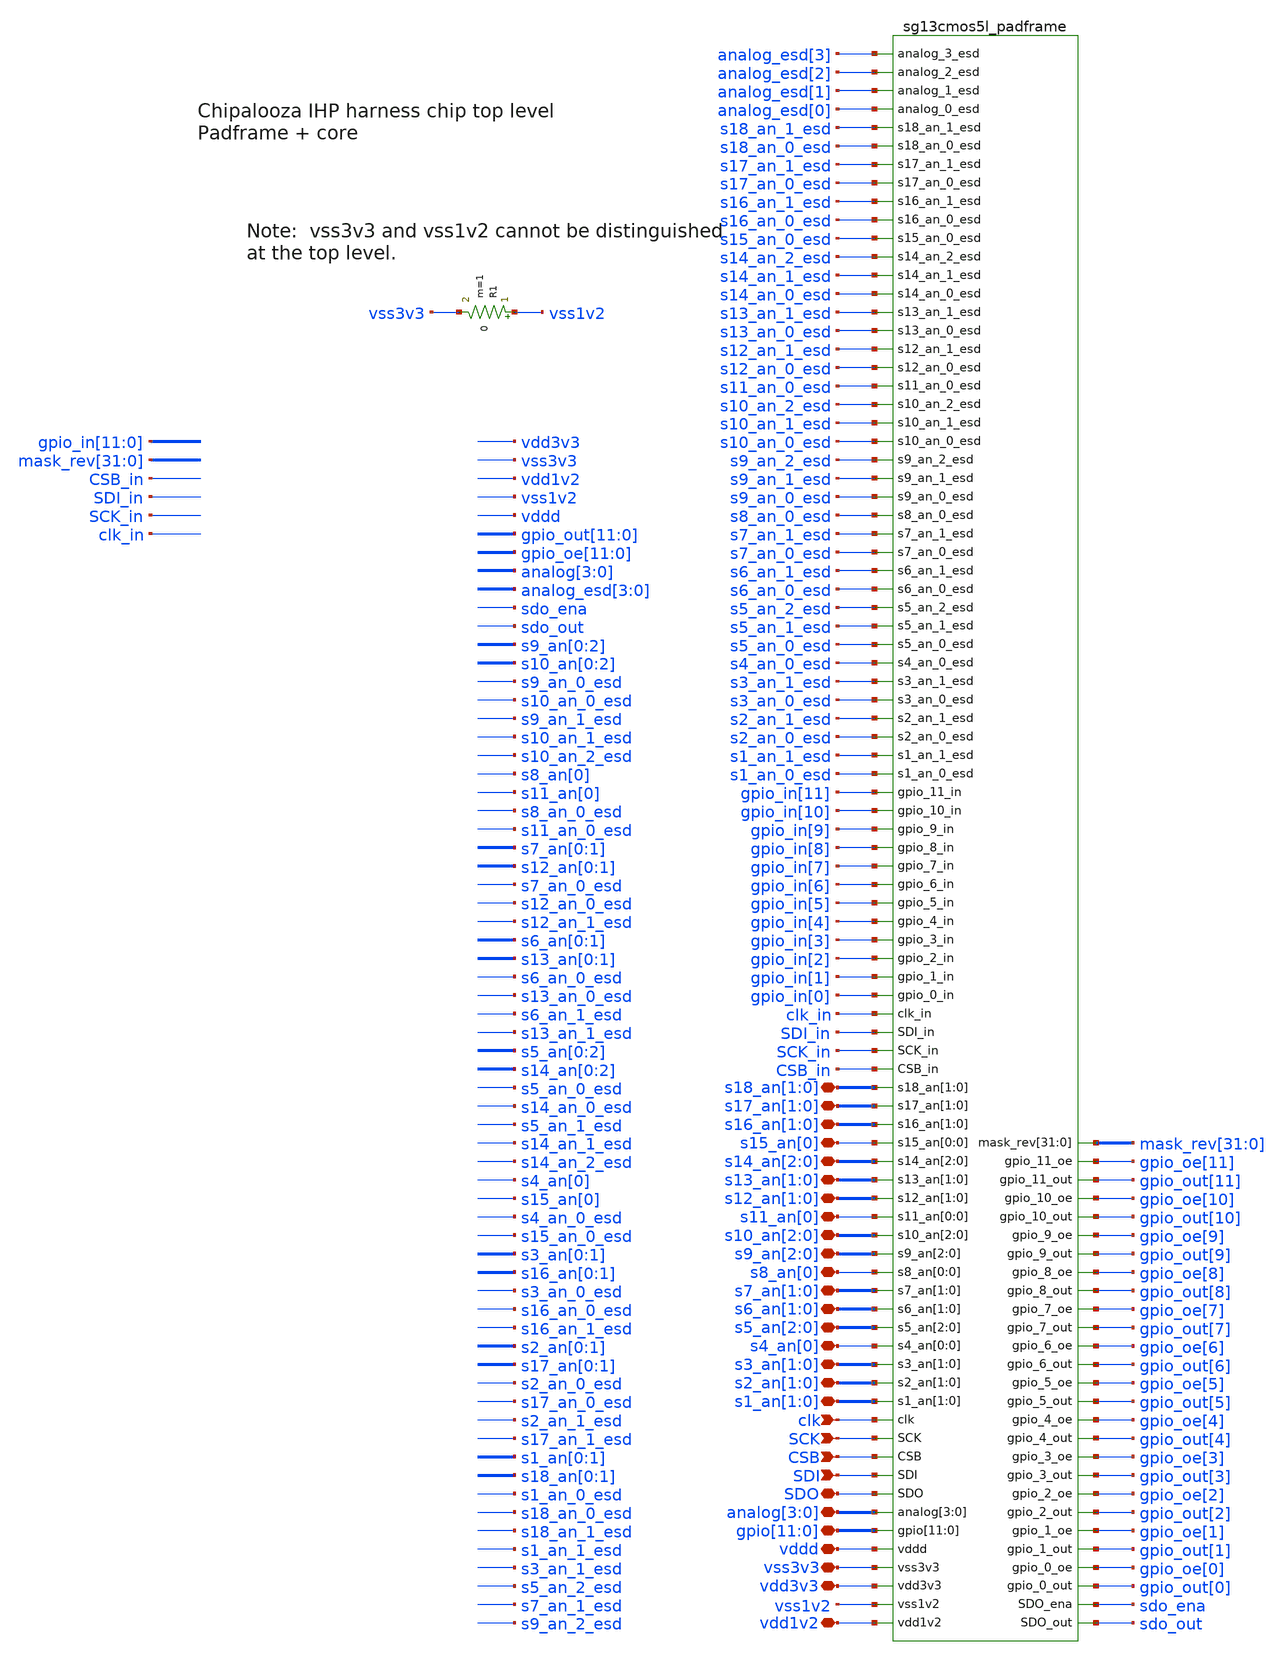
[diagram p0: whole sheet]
** sch_path: xschem/sg13cmos5l_ocd_chipalooza.sch
**.subckt sg13cmos5l_ocd_chipalooza SDO analog[3],analog[2],analog[1],analog[0]
*+ gpio[11],gpio[10],gpio[9],gpio[8],gpio[7],gpio[6],gpio[5],gpio[4],gpio[3],gpio[2],gpio[1],gpio[0] vdd3v3 vss3v3 vdd1v2 vddd SDI SCK clk CSB s18_an[1],s18_an[0] s17_an[1],s17_an[0]
*+ s16_an[1],s16_an[0] s15_an[0] s14_an[2],s14_an[1],s14_an[0] s13_an[1],s13_an[0] s12_an[1],s12_an[0] s11_an[0]
*+ s10_an[2],s10_an[1],s10_an[0] s9_an[2],s9_an[1],s9_an[0] s8_an[0] s7_an[1],s7_an[0] s6_an[1],s6_an[0] s5_an[2],s5_an[1],s5_an[0]
*+ s4_an[0] s3_an[1],s3_an[0] s2_an[1],s2_an[0] s1_an[1],s1_an[0]
*.iopin SDO
*.iopin analog[3],analog[2],analog[1],analog[0]
*.iopin
*+ gpio[11],gpio[10],gpio[9],gpio[8],gpio[7],gpio[6],gpio[5],gpio[4],gpio[3],gpio[2],gpio[1],gpio[0]
*.iopin vdd3v3
*.iopin vss3v3
*.iopin vdd1v2
*.iopin vddd
*.ipin SDI
*.ipin SCK
*.ipin clk
*.ipin CSB
*.iopin s18_an[1],s18_an[0]
*.iopin s17_an[1],s17_an[0]
*.iopin s16_an[1],s16_an[0]
*.iopin s15_an[0]
*.iopin s14_an[2],s14_an[1],s14_an[0]
*.iopin s13_an[1],s13_an[0]
*.iopin s12_an[1],s12_an[0]
*.iopin s11_an[0]
*.iopin s10_an[2],s10_an[1],s10_an[0]
*.iopin s9_an[2],s9_an[1],s9_an[0]
*.iopin s8_an[0]
*.iopin s7_an[1],s7_an[0]
*.iopin s6_an[1],s6_an[0]
*.iopin s5_an[2],s5_an[1],s5_an[0]
*.iopin s4_an[0]
*.iopin s3_an[1],s3_an[0]
*.iopin s2_an[1],s2_an[0]
*.iopin s1_an[1],s1_an[0]
x1 vdd1v2 vss1v2 vdd3v3 vss3v3 vddd gpio[11] gpio[10] gpio[9] gpio[8] gpio[7] gpio[6] gpio[5]
+ gpio[4] gpio[3] gpio[2] gpio[1] gpio[0] analog[3] analog[2] analog[1] analog[0] SDO SDI CSB SCK clk
+ s1_an[1] s1_an[0] s2_an[1] s2_an[0] s3_an[1] s3_an[0] s4_an[0] s5_an[2] s5_an[1] s5_an[0] s6_an[1] s6_an[0]
+ s7_an[1] s7_an[0] s8_an[0] s9_an[2] s9_an[1] s9_an[0] s10_an[2] s10_an[1] s10_an[0] s11_an[0] s12_an[1]
+ s12_an[0] s13_an[1] s13_an[0] s14_an[2] s14_an[1] s14_an[0] s15_an[0] s16_an[1] s16_an[0] s17_an[1] s17_an[0]
+ s18_an[1] s18_an[0] sdo_out sdo_ena CSB_in SCK_in SDI_in clk_in gpio_in[0] gpio_out[0] gpio_oe[0] gpio_in[1]
+ gpio_out[1] gpio_oe[1] gpio_in[2] gpio_out[2] gpio_oe[2] gpio_in[3] gpio_out[3] gpio_oe[3] gpio_in[4]
+ gpio_out[4] gpio_oe[4] gpio_in[5] gpio_out[5] gpio_oe[5] gpio_in[6] gpio_out[6] gpio_oe[6] gpio_in[7]
+ gpio_out[7] gpio_oe[7] gpio_in[8] gpio_out[8] gpio_oe[8] gpio_in[9] gpio_out[9] gpio_oe[9] gpio_in[10]
+ gpio_out[10] gpio_oe[10] gpio_in[11] gpio_out[11] gpio_oe[11] s1_an_0_esd s1_an_1_esd s2_an_0_esd s2_an_1_esd
+ s3_an_0_esd s3_an_1_esd s4_an_0_esd s5_an_0_esd s5_an_1_esd s5_an_2_esd s6_an_0_esd s6_an_1_esd s7_an_0_esd
+ s7_an_1_esd s8_an_0_esd s9_an_0_esd s9_an_1_esd s9_an_2_esd s10_an_0_esd s10_an_1_esd s10_an_2_esd s11_an_0_esd
+ s12_an_0_esd s12_an_1_esd s13_an_0_esd s13_an_1_esd s14_an_0_esd s14_an_1_esd s14_an_2_esd s15_an_0_esd
+ s16_an_0_esd s16_an_1_esd s17_an_0_esd s17_an_1_esd s18_an_0_esd s18_an_1_esd analog_esd[0] analog_esd[1]
+ analog_esd[2] analog_esd[3] mask_rev[31] mask_rev[30] mask_rev[29] mask_rev[28] mask_rev[27] mask_rev[26]
+ mask_rev[25] mask_rev[24] mask_rev[23] mask_rev[22] mask_rev[21] mask_rev[20] mask_rev[19] mask_rev[18]
+ mask_rev[17] mask_rev[16] mask_rev[15] mask_rev[14] mask_rev[13] mask_rev[12] mask_rev[11] mask_rev[10]
+ mask_rev[9] mask_rev[8] mask_rev[7] mask_rev[6] mask_rev[5] mask_rev[4] mask_rev[3] mask_rev[2] mask_rev[1]
+ mask_rev[0] sg13cmos5l_padframe
R1 vss1v2 vss3v3 0 m=1
**.ends
.end
